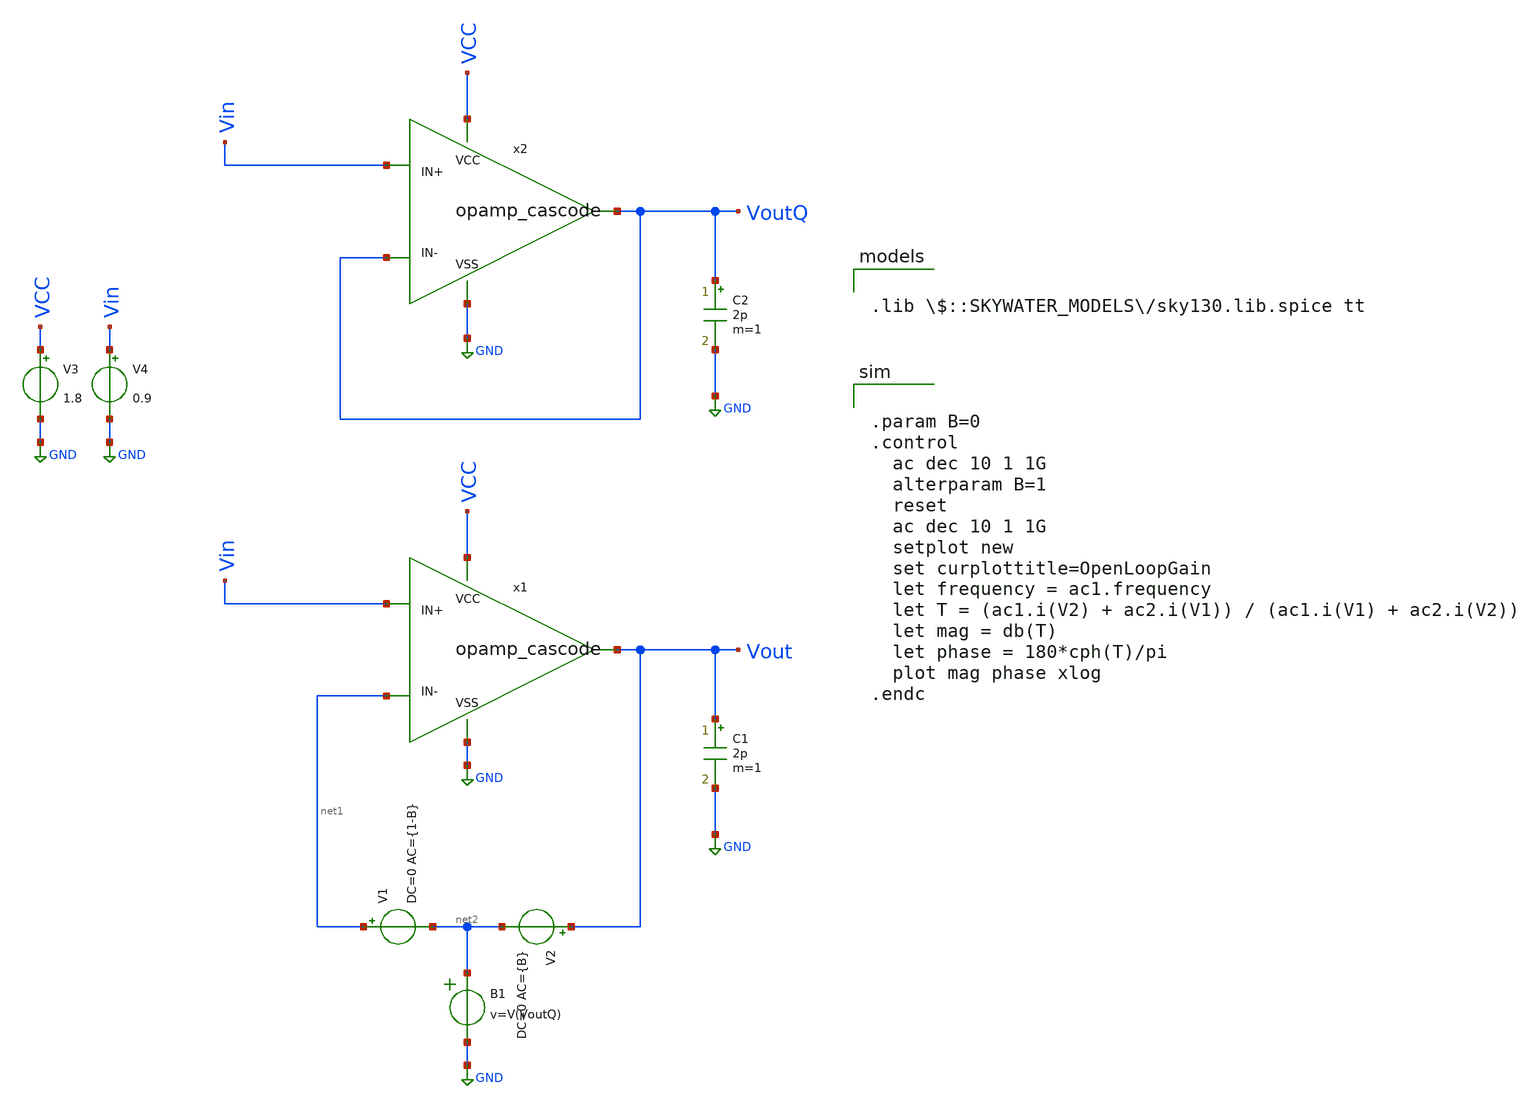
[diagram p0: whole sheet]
** sch_path: opamp_cascode_test_ac.sch
**.subckt opamp_cascode_test_ac
V3 VCC GND 1.8
V4 Vin GND 0.9
V2 Vout net2 DC=0 AC={B}
C1 Vout GND 2p m=1
C2 VoutQ GND 2p m=1
V1 net1 net2 DC=0 AC={1-B}
B1 net2 GND v=V(VoutQ)
x2 VCC GND Vin VoutQ VoutQ opamp_cascode
x1 VCC GND Vin net1 Vout opamp_cascode
**** begin user architecture code


.param B=0
.control
  ac dec 10 1 1G
  alterparam B=1
  reset
  ac dec 10 1 1G
  setplot new
  set curplottitle=OpenLoopGain
  let frequency = ac1.frequency
  let T = (ac1.i(V2) + ac2.i(V1)) / (ac1.i(V1) + ac2.i(V2))
  let mag = db(T)
  let phase = 180*cph(T)/pi
  plot mag phase xlog
.endc



.lib $::SKYWATER_MODELS/sky130.lib.spice tt

**** end user architecture code
**.ends

* expanding   symbol:  /home/zwierzak/projects/SKY130_OpAmp_GIT/opamp_cascode.sym # of pins=5
** sym_path: opamp_cascode.sym
** sch_path: opamp_cascode.sch
.subckt opamp_cascode VCC VSS IN+ IN- OUT
*.ipin IN+
*.ipin IN-
*.ipin VCC
*.ipin VSS
*.opin OUT
XM10 net8 net6 VCC VCC sky130_fd_pr__pfet_01v8 L=10 W=5 nf=1 ad='int((nf+1)/2) * W/nf * 0.29' as='int((nf+2)/2) * W/nf * 0.29'
+ pd='2*int((nf+1)/2) * (W/nf + 0.29)' ps='2*int((nf+2)/2) * (W/nf + 0.29)' nrd='0.29 / W' nrs='0.29 / W'
+ sa=0 sb=0 sd=0 mult=30 m=30
XM1 net7 net6 VCC VCC sky130_fd_pr__pfet_01v8 L=10 W=5 nf=1 ad='int((nf+1)/2) * W/nf * 0.29' as='int((nf+2)/2) * W/nf * 0.29'
+ pd='2*int((nf+1)/2) * (W/nf + 0.29)' ps='2*int((nf+2)/2) * (W/nf + 0.29)' nrd='0.29 / W' nrs='0.29 / W'
+ sa=0 sb=0 sd=0 mult=30 m=30
XM5 net3 net9 VCC VCC sky130_fd_pr__pfet_01v8 L=3 W=5 nf=1 ad='int((nf+1)/2) * W/nf * 0.29' as='int((nf+2)/2) * W/nf * 0.29'
+ pd='2*int((nf+1)/2) * (W/nf + 0.29)' ps='2*int((nf+2)/2) * (W/nf + 0.29)' nrd='0.29 / W' nrs='0.29 / W'
+ sa=0 sb=0 sd=0 mult=40 m=40
XM100 net9 net9 VCC VCC sky130_fd_pr__pfet_01v8 L=3 W=5 nf=1 ad='int((nf+1)/2) * W/nf * 0.29' as='int((nf+2)/2) * W/nf * 0.29'
+ pd='2*int((nf+1)/2) * (W/nf + 0.29)' ps='2*int((nf+2)/2) * (W/nf + 0.29)' nrd='0.29 / W' nrs='0.29 / W'
+ sa=0 sb=0 sd=0 mult=4 m=4
I0 net9 VSS 5.1u
XM11 OUT BIAS net8 net8 sky130_fd_pr__pfet_01v8 L=5 W=5 nf=1 ad='int((nf+1)/2) * W/nf * 0.29' as='int((nf+2)/2) * W/nf * 0.29'
+ pd='2*int((nf+1)/2) * (W/nf + 0.29)' ps='2*int((nf+2)/2) * (W/nf + 0.29)' nrd='0.29 / W' nrs='0.29 / W'
+ sa=0 sb=0 sd=0 mult=12 m=12
XM2 net6 BIAS net7 net7 sky130_fd_pr__pfet_01v8 L=5 W=5 nf=1 ad='int((nf+1)/2) * W/nf * 0.29' as='int((nf+2)/2) * W/nf * 0.29'
+ pd='2*int((nf+1)/2) * (W/nf + 0.29)' ps='2*int((nf+2)/2) * (W/nf + 0.29)' nrd='0.29 / W' nrs='0.29 / W'
+ sa=0 sb=0 sd=0 mult=12 m=12
XM6 net1 IN- net3 net3 sky130_fd_pr__pfet_01v8 L=0.18 W=5 nf=1 ad='int((nf+1)/2) * W/nf * 0.29' as='int((nf+2)/2) * W/nf * 0.29'
+ pd='2*int((nf+1)/2) * (W/nf + 0.29)' ps='2*int((nf+2)/2) * (W/nf + 0.29)' nrd='0.29 / W' nrs='0.29 / W'
+ sa=0 sb=0 sd=0 mult=50 m=50
XM8 net2 IN+ net3 net3 sky130_fd_pr__pfet_01v8 L=0.18 W=5 nf=1 ad='int((nf+1)/2) * W/nf * 0.29' as='int((nf+2)/2) * W/nf * 0.29'
+ pd='2*int((nf+1)/2) * (W/nf + 0.29)' ps='2*int((nf+2)/2) * (W/nf + 0.29)' nrd='0.29 / W' nrs='0.29 / W'
+ sa=0 sb=0 sd=0 mult=50 m=50
XM7 net1 net1 VSS VSS sky130_fd_pr__nfet_01v8 L=1 W=5 nf=1 ad='int((nf+1)/2) * W/nf * 0.29' as='int((nf+2)/2) * W/nf * 0.29'
+ pd='2*int((nf+1)/2) * (W/nf + 0.29)' ps='2*int((nf+2)/2) * (W/nf + 0.29)' nrd='0.29 / W' nrs='0.29 / W'
+ sa=0 sb=0 sd=0 mult=3 m=3
XM9 net2 net2 VSS VSS sky130_fd_pr__nfet_01v8 L=1 W=5 nf=1 ad='int((nf+1)/2) * W/nf * 0.29' as='int((nf+2)/2) * W/nf * 0.29'
+ pd='2*int((nf+1)/2) * (W/nf + 0.29)' ps='2*int((nf+2)/2) * (W/nf + 0.29)' nrd='0.29 / W' nrs='0.29 / W'
+ sa=0 sb=0 sd=0 mult=3 m=3
XM13 net4 net2 VSS VSS sky130_fd_pr__nfet_01v8 L=1 W=5 nf=1 ad='int((nf+1)/2) * W/nf * 0.29' as='int((nf+2)/2) * W/nf * 0.29'
+ pd='2*int((nf+1)/2) * (W/nf + 0.29)' ps='2*int((nf+2)/2) * (W/nf + 0.29)' nrd='0.29 / W' nrs='0.29 / W'
+ sa=0 sb=0 sd=0 mult=6 m=6
XM4 net5 net1 VSS VSS sky130_fd_pr__nfet_01v8 L=1 W=5 nf=1 ad='int((nf+1)/2) * W/nf * 0.29' as='int((nf+2)/2) * W/nf * 0.29'
+ pd='2*int((nf+1)/2) * (W/nf + 0.29)' ps='2*int((nf+2)/2) * (W/nf + 0.29)' nrd='0.29 / W' nrs='0.29 / W'
+ sa=0 sb=0 sd=0 mult=6 m=6
XM12 OUT BIAS1 net4 net4 sky130_fd_pr__nfet_01v8 L=3 W=5 nf=1 ad='int((nf+1)/2) * W/nf * 0.29' as='int((nf+2)/2) * W/nf * 0.29'
+ pd='2*int((nf+1)/2) * (W/nf + 0.29)' ps='2*int((nf+2)/2) * (W/nf + 0.29)' nrd='0.29 / W' nrs='0.29 / W'
+ sa=0 sb=0 sd=0 mult=9 m=9
XM3 net6 BIAS1 net5 net5 sky130_fd_pr__nfet_01v8 L=3 W=5 nf=1 ad='int((nf+1)/2) * W/nf * 0.29' as='int((nf+2)/2) * W/nf * 0.29'
+ pd='2*int((nf+1)/2) * (W/nf + 0.29)' ps='2*int((nf+2)/2) * (W/nf + 0.29)' nrd='0.29 / W' nrs='0.29 / W'
+ sa=0 sb=0 sd=0 mult=9 m=9
V1 BIAS VSS 0.12
V2 BIAS1 VSS 0.7
.ends

.GLOBAL GND
.end
